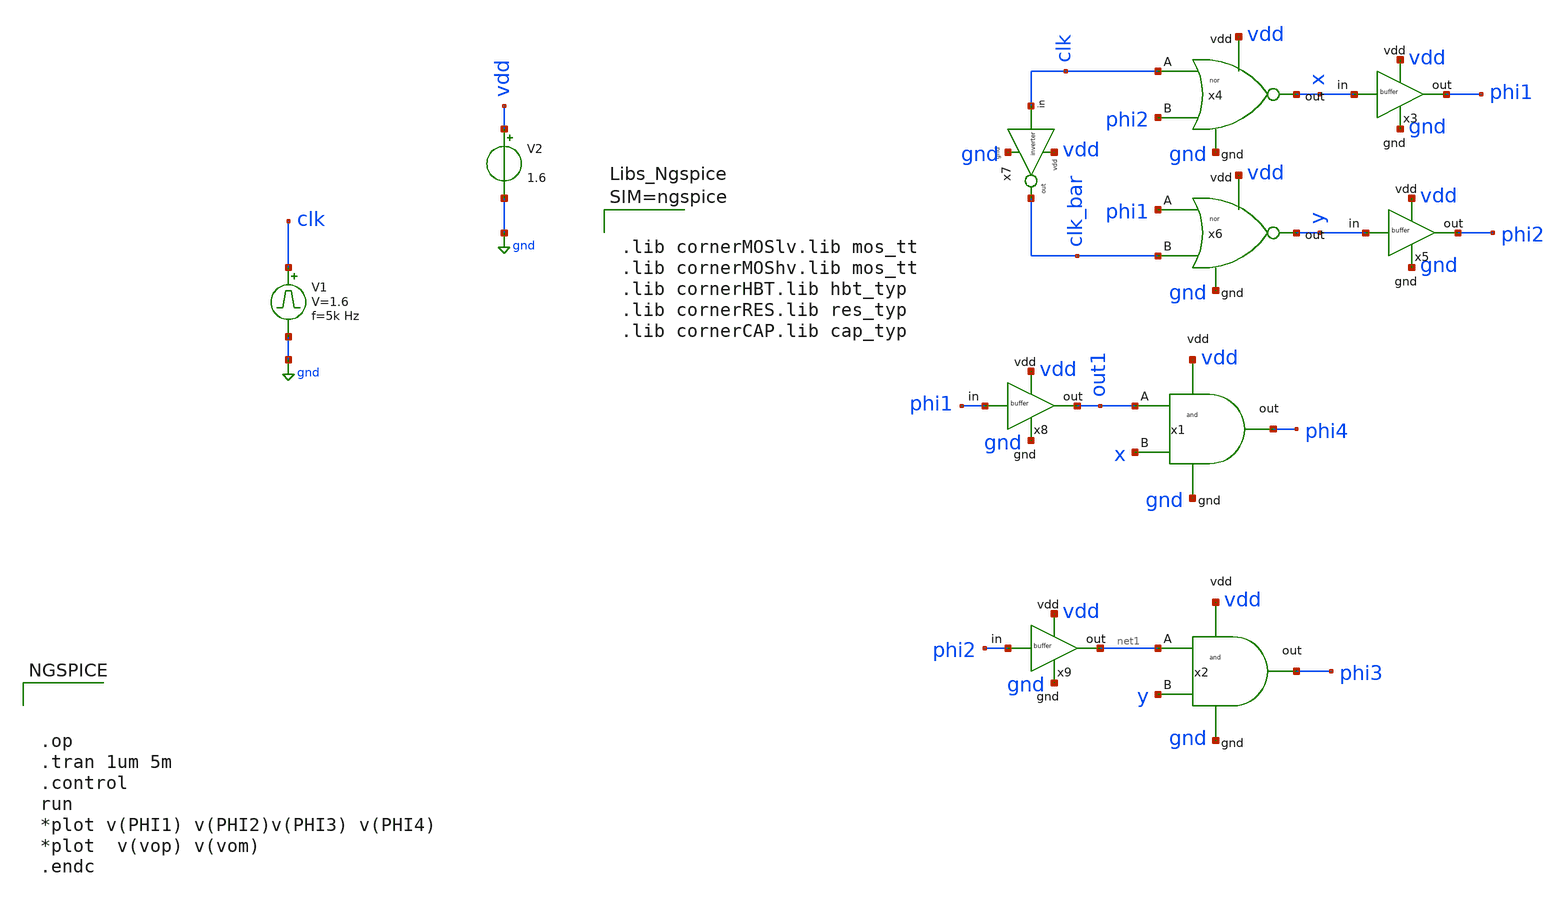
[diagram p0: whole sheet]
** sch_path: Clock_gen_using_transistor_hv/top_module.sch
**.subckt top_module
x1 vdd x out1 gnd phi4 and
x2 vdd y net1 gnd phi3 and
x4 vdd phi2 clk gnd x nor
x6 vdd clk_bar phi1 gnd y nor
x7 clk clk_bar vdd gnd inverter
x8 phi1 out1 vdd gnd buffer
x9 phi2 net1 vdd gnd buffer
V2 vdd gnd 1.6
V1 clk gnd pulse 0 1.6 '0.495/ 5k ' '0.01/5k ' '0.01/5k ' '0.49/5k ' '1/5k '
x3 x phi1 vdd gnd buffer
x5 y phi2 vdd gnd buffer
**** begin user architecture code



.lib cornerMOSlv.lib mos_tt
.lib cornerMOShv.lib mos_tt
.lib cornerHBT.lib hbt_typ
.lib cornerRES.lib res_typ
.lib cornerCAP.lib cap_typ






.op
.tran 1um 5m
.control
run
*plot v(PHI1) v(PHI2)v(PHI3) v(PHI4)
*plot  v(vop) v(vom)
.endc


**** end user architecture code
**.ends

* expanding   symbol:
*+  /home/designer/shared/uni_cass/final_Design_file/Clock_gen_using_transistor_hv/and.sym # of pins=5
** sym_path: /home/designer/shared/uni_cass/final_Design_file/Clock_gen_using_transistor_hv/and.sym
** sch_path: /home/designer/shared/uni_cass/final_Design_file/Clock_gen_using_transistor_hv/and.sch
.subckt and vdd B A gnd out
*.iopin vdd
*.iopin B
*.iopin A
*.iopin gnd
*.iopin out
XM3 net1 A vdd vdd sg13_hv_pmos w=0.3u l=0.45u ng=1 m=1 mm_ok=1
XM1 net2 B gnd gnd sg13_hv_nmos w=0.3u l=0.45u ng=1 m=1 mm_ok=1
XM2 net1 A net2 net2 sg13_hv_nmos w=0.3u l=0.45u ng=1 m=1 mm_ok=1
XM4 net1 B vdd vdd sg13_hv_pmos w=0.3u l=0.45u ng=1 m=1 mm_ok=1
XM5 out net1 vdd vdd sg13_hv_pmos w=0.3u l=0.45u ng=1 m=1 mm_ok=1
XM6 out net1 gnd gnd sg13_hv_nmos w=0.3u l=0.45u ng=1 m=1 mm_ok=1
.ends


* expanding   symbol:
*+  /home/designer/shared/uni_cass/final_Design_file/Clock_gen_using_transistor_hv/nor.sym # of pins=5
** sym_path: /home/designer/shared/uni_cass/final_Design_file/Clock_gen_using_transistor_hv/nor.sym
** sch_path: /home/designer/shared/uni_cass/final_Design_file/Clock_gen_using_transistor_hv/nor.sch
.subckt nor vdd B A gnd out
*.iopin vdd
*.iopin B
*.iopin A
*.iopin gnd
*.iopin out
XM3 net1 A vdd vdd sg13_hv_pmos w=0.3u l=0.45u ng=1 m=1 mm_ok=1
XM1 out B gnd gnd sg13_hv_nmos w=0.3u l=0.45u ng=1 m=1 mm_ok=1
XM2 out A gnd gnd sg13_hv_nmos w=0.3u l=0.45u ng=1 m=1 mm_ok=1
XM4 out B net1 net1 sg13_hv_pmos w=0.3u l=0.45u ng=1 m=1 mm_ok=1
.ends


* expanding   symbol:
*+  /home/designer/shared/uni_cass/final_Design_file/Clock_gen_using_transistor_hv/inverter.sym # of pins=4
** sym_path: /home/designer/shared/uni_cass/final_Design_file/Clock_gen_using_transistor_hv/inverter.sym
** sch_path: /home/designer/shared/uni_cass/final_Design_file/Clock_gen_using_transistor_hv/inverter.sch
.subckt inverter in out vdd gnd
*.iopin in
*.iopin vdd
*.iopin out
*.iopin gnd
XM3 out in vdd vdd sg13_hv_pmos w=2u l=2u ng=1 m=1 mm_ok=1
XM1 out in gnd gnd sg13_hv_nmos w=1u l=1u ng=1 m=1 mm_ok=1
.ends


* expanding   symbol:
*+  /home/designer/shared/uni_cass/final_Design_file/Clock_gen_using_transistor_hv/buffer.sym # of pins=4
** sym_path: /home/designer/shared/uni_cass/final_Design_file/Clock_gen_using_transistor_hv/buffer.sym
** sch_path: /home/designer/shared/uni_cass/final_Design_file/Clock_gen_using_transistor_hv/buffer.sch
.subckt buffer in out vdd gnd
*.iopin in
*.iopin out
*.iopin vdd
*.iopin gnd
x1 in net1 vdd gnd inverter
x2 net1 net2 vdd gnd inverter
x3 net2 net3 vdd gnd inverter
x4 net3 net9 vdd gnd inverter
x5 net9 net4 vdd gnd inverter
x6 net4 net5 vdd gnd inverter
x7 net5 net10 vdd gnd inverter
x8 net10 net6 vdd gnd inverter
x9 net6 net11 vdd gnd inverter
x10 net11 net7 vdd gnd inverter
x11 net7 net8 vdd gnd inverter
x12 net8 out vdd gnd inverter
.ends

.GLOBAL gnd
.end
